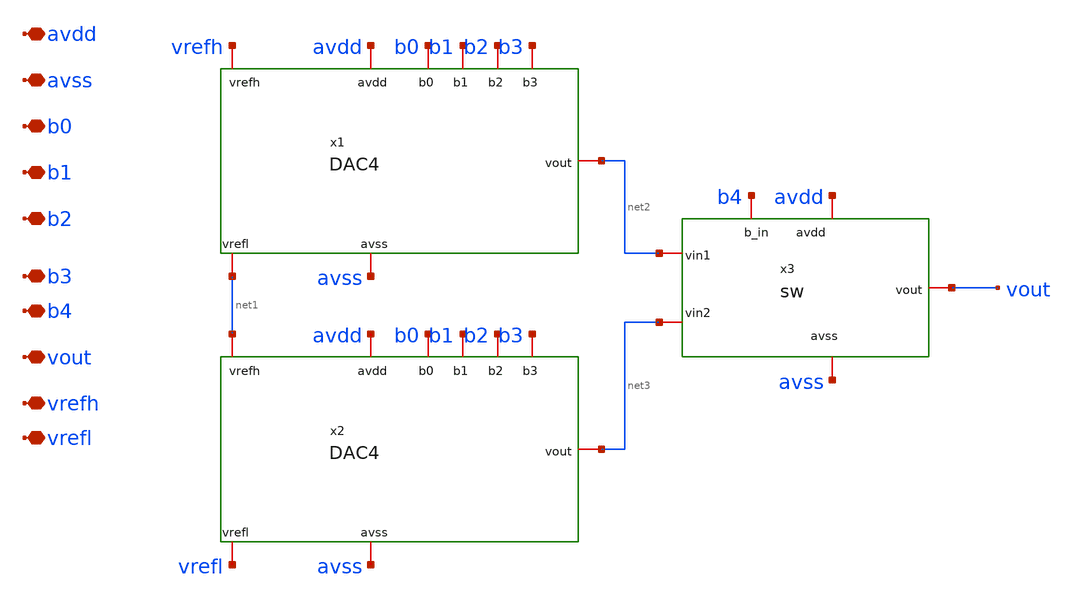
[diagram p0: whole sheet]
** sch_path: designs/libs/crossmem_ipn/dac4bits/sch/DAC5.sch
**.subckt DAC5 avdd avss b0 b1 b2 b3 vout b4 vrefh vrefl
*.iopin avdd
*.iopin avss
*.iopin b0
*.iopin b1
*.iopin b2
*.iopin b3
*.iopin vout
*.iopin b4
*.iopin vrefh
*.iopin vrefl
x1 avdd b0 b1 avss b2 vrefh net2 net1 b3 DAC4
x3 avdd b4 avss net2 vout net3 sw
x2 avdd b0 b1 avss b2 net1 net3 vrefl b3 DAC4
**.ends

* expanding   symbol:  DAC4.sym # of pins=9
** sym_path: designs/libs/crossmem_ipn/dac4bits/sch/DAC4.sym
** sch_path: designs/libs/crossmem_ipn/dac4bits/sch/DAC4.sch
.subckt DAC4 avdd b0 b1 avss b2 vrefh vout vrefl b3
*.iopin avdd
*.iopin avss
*.iopin b0
*.iopin b1
*.iopin b2
*.iopin vout
*.iopin b3
*.iopin vrefh
*.iopin vrefl
x1 avdd b0 b1 avss b2 vrefh net2 net1 DAC3
x2 avdd b0 b1 avss b2 net1 net3 vrefl DAC3
x3 avdd b3 avss net2 vout net3 sw
.ends


* expanding   symbol:  sw.sym # of pins=6
** sym_path: designs/libs/crossmem_ipn/dac4bits/sch/sw.sym
** sch_path: designs/libs/crossmem_ipn/dac4bits/sch/sw.sch
.subckt sw avdd b_in avss vin1 vout vin2
*.iopin avss
*.iopin vin1
*.iopin vout
*.iopin avdd
*.iopin vin2
*.iopin b_in
XM1 net1 b_in avss avss sky130_fd_pr__nfet_01v8 L=0.15 W=0.5 nf=1 ad='int((nf+1)/2) * W/nf * 0.29' as='int((nf+2)/2) * W/nf * 0.29'
+ pd='2*int((nf+1)/2) * (W/nf + 0.29)' ps='2*int((nf+2)/2) * (W/nf + 0.29)' nrd='0.29 / W' nrs='0.29 / W'
+ sa=0 sb=0 sd=0 mult=1 m=1
XM2 net1 b_in avdd avdd sky130_fd_pr__pfet_01v8 L=0.15 W=0.5 nf=1 ad='int((nf+1)/2) * W/nf * 0.29' as='int((nf+2)/2) * W/nf * 0.29'
+ pd='2*int((nf+1)/2) * (W/nf + 0.29)' ps='2*int((nf+2)/2) * (W/nf + 0.29)' nrd='0.29 / W' nrs='0.29 / W'
+ sa=0 sb=0 sd=0 mult=1 m=1
XM3 net2 net1 avss avss sky130_fd_pr__nfet_01v8 L=0.15 W=0.5 nf=1 ad='int((nf+1)/2) * W/nf * 0.29' as='int((nf+2)/2) * W/nf * 0.29'
+ pd='2*int((nf+1)/2) * (W/nf + 0.29)' ps='2*int((nf+2)/2) * (W/nf + 0.29)' nrd='0.29 / W' nrs='0.29 / W'
+ sa=0 sb=0 sd=0 mult=1 m=1
XM4 net2 net1 avdd avdd sky130_fd_pr__pfet_01v8 L=0.15 W=0.5 nf=1 ad='int((nf+1)/2) * W/nf * 0.29' as='int((nf+2)/2) * W/nf * 0.29'
+ pd='2*int((nf+1)/2) * (W/nf + 0.29)' ps='2*int((nf+2)/2) * (W/nf + 0.29)' nrd='0.29 / W' nrs='0.29 / W'
+ sa=0 sb=0 sd=0 mult=1 m=1
XM5 vout net1 vin1 avdd sky130_fd_pr__pfet_01v8 L=0.15 W=0.5 nf=1 ad='int((nf+1)/2) * W/nf * 0.29' as='int((nf+2)/2) * W/nf * 0.29'
+ pd='2*int((nf+1)/2) * (W/nf + 0.29)' ps='2*int((nf+2)/2) * (W/nf + 0.29)' nrd='0.29 / W' nrs='0.29 / W'
+ sa=0 sb=0 sd=0 mult=1 m=1
XM6 vout net1 vin2 avss sky130_fd_pr__nfet_01v8 L=0.15 W=0.5 nf=1 ad='int((nf+1)/2) * W/nf * 0.29' as='int((nf+2)/2) * W/nf * 0.29'
+ pd='2*int((nf+1)/2) * (W/nf + 0.29)' ps='2*int((nf+2)/2) * (W/nf + 0.29)' nrd='0.29 / W' nrs='0.29 / W'
+ sa=0 sb=0 sd=0 mult=1 m=1
XM7 vin1 net2 vout avss sky130_fd_pr__nfet_01v8 L=0.15 W=0.5 nf=1 ad='int((nf+1)/2) * W/nf * 0.29' as='int((nf+2)/2) * W/nf * 0.29'
+ pd='2*int((nf+1)/2) * (W/nf + 0.29)' ps='2*int((nf+2)/2) * (W/nf + 0.29)' nrd='0.29 / W' nrs='0.29 / W'
+ sa=0 sb=0 sd=0 mult=1 m=1
XM8 vin2 net2 vout avdd sky130_fd_pr__pfet_01v8 L=0.15 W=0.5 nf=1 ad='int((nf+1)/2) * W/nf * 0.29' as='int((nf+2)/2) * W/nf * 0.29'
+ pd='2*int((nf+1)/2) * (W/nf + 0.29)' ps='2*int((nf+2)/2) * (W/nf + 0.29)' nrd='0.29 / W' nrs='0.29 / W'
+ sa=0 sb=0 sd=0 mult=1 m=1
.ends


* expanding   symbol:  /foss/designs/crossmem_ipn/designs/libs/crossmem_ipn/dac4bits/sch/DAC3.sym #
*+ of pins=8
** sym_path: designs/libs/crossmem_ipn/dac4bits/sch/DAC3.sym
** sch_path: designs/libs/crossmem_ipn/dac4bits/sch/DAC3.sch
.subckt DAC3 avdd b0 b1 avss b2 vrefh vout vrefl
*.iopin vrefh
*.iopin vrefl
*.iopin b0
*.iopin b1
*.iopin b2
*.iopin avdd
*.iopin avss
*.iopin vout
x1 b0 avdd b1 avss vrefh net1 net3 DAC2BIT
x2 b0 avdd b1 avss net3 net2 vrefl DAC2BIT
x3 avdd b2 avss net1 vout net2 sw
.ends


* expanding   symbol:  /foss/designs/crossmem_ipn/designs/libs/crossmem_ipn/dac4bits/sch/DAC2BIT.sym
*+ # of pins=7
** sym_path: designs/libs/crossmem_ipn/dac4bits/sch/DAC2BIT.sym
** sch_path: designs/libs/crossmem_ipn/dac4bits/sch/DAC2BIT.sch
.subckt DAC2BIT b0 avdd b1 avss vrefh vout vrefl
*.iopin vrefh
*.iopin vrefl
*.iopin b0
*.iopin b1
*.iopin avdd
*.iopin avss
*.iopin vout
x1 avdd b0 avss net5 net1 net4 sw
x2 avdd b0 avss net3 net2 vrefl sw
x3 avdd b1 avss net1 vout net2 sw
R5 net5 vrefh sky130_fd_pr__res_generic_l1 W=1 L=3.75 m=1
R6 net4 net5 sky130_fd_pr__res_generic_l1 W=1 L=3.75 m=1
R7 net3 net4 sky130_fd_pr__res_generic_l1 W=1 L=3.75 m=1
R8 vrefl net3 sky130_fd_pr__res_generic_l1 W=1 L=3.75 m=1
.ends

.end
